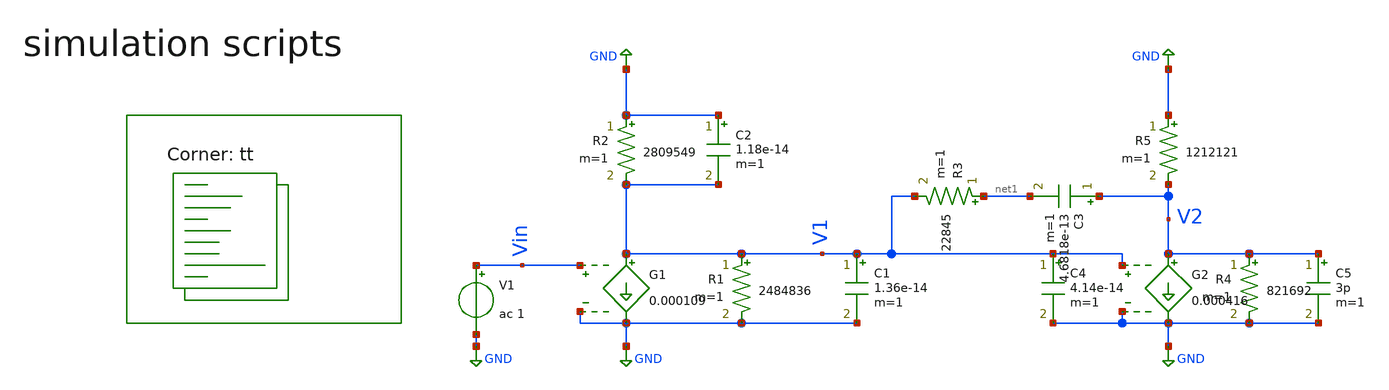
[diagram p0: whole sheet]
** sch_path: Learning/single_ended_amplifiers/Miller_OTA_2_stage_model/simplified_diff_gain_model.sch
**.subckt simplified_diff_gain_model
G1 V1 GND Vin GND 0.000109
C1 V1 GND 1.36e-14 m=1
R1 V1 GND 2484836 m=1
G2 V2 GND V1 GND 0.000416
R3 net1 V1 22845 m=1
C3 V2 net1 4.6818e-13 m=1
R5 GND V2 1212121 m=1
C5 V2 GND 3p m=1
R4 V2 GND 821692 m=1
V1 Vin GND ac 1
C2 GND V1 1.18e-14 m=1
C4 V1 GND 4.14e-14 m=1
R2 GND V1 2809549 m=1
**** begin user architecture code
.lib $::SKYWATER_MODELS/sky130.lib.spice tt

.Temp 27
.param VDD = 5
.param VSS = 0



.control
save all
ac dec 100 1 10G
plot db(v(V2)) (180+(180*ph(v(V2))/pi)) db(v(V1))
pz VIN 0 0 V2 vol pz
print all




.endc


**** end user architecture code
**.ends
.GLOBAL GND
.end
